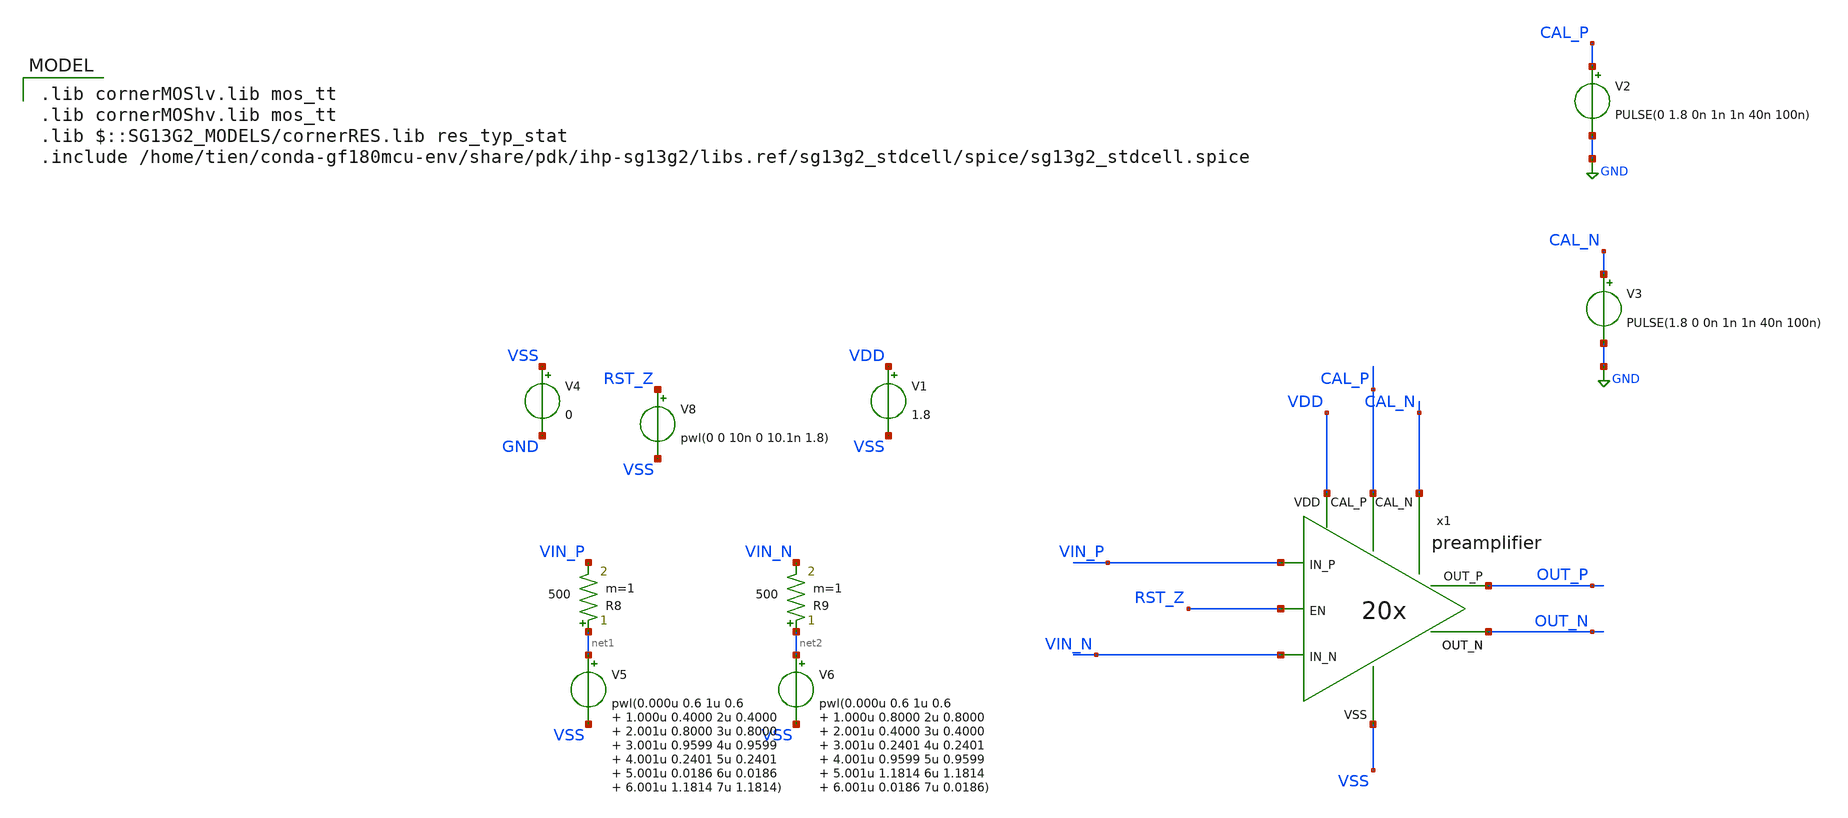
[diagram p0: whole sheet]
** sch_path: schematic/simulations/preamplifier_tb.sch
**.subckt preamplifier_tb
V8 RST_Z VSS pwl(0 0 10n 0 10.1n 1.8)
V1 VDD VSS 1.8
.save i(v1)
V4 VSS GND 0
V5 net1 VSS pwl(0.000u 0.6 1u 0.6 1.000u 0.4000 2u 0.4000 2.001u 0.8000 3u 0.8000 3.001u 0.9599 4u
+ 0.9599 4.001u 0.2401 5u 0.2401 5.001u 0.0186 6u 0.0186 6.001u 1.1814 7u 1.1814)
V6 net2 VSS pwl(0.000u 0.6 1u 0.6 1.000u 0.8000 2u 0.8000 2.001u 0.4000 3u 0.4000 3.001u 0.2401 4u
+ 0.2401 4.001u 0.9599 5u 0.9599 5.001u 1.1814 6u 1.1814 6.001u 0.0186 7u 0.0186)
R8 net1 VIN_P 500 m=1
R9 net2 VIN_N 500 m=1
V2 CAL_P GND PULSE(0 1.8 0n 1n 1n 40n 100n)
V3 CAL_N GND PULSE(1.8 0 0n 1n 1n 40n 100n)
x1 VIN_N VIN_P VDD RST_Z OUT_P OUT_N VSS CAL_P CAL_N preamplifier
**** begin user architecture code
 .lib cornerMOSlv.lib mos_tt
.lib cornerMOShv.lib mos_tt
.lib $::SG13G2_MODELS/cornerRES.lib res_typ_stat
.include /home/tien/conda-gf180mcu-env/share/pdk/ihp-sg13g2/libs.ref/sg13g2_stdcell/spice/sg13g2_stdcell.spice




.option temp = 27
.save all

.option GMIN=1e-12 reltol=1e-6

.tran 10n 10u


**** end user architecture code
**.ends

* expanding   symbol:  preamplifier/preamplifier.sym # of pins=9
** sym_path: schematic/preamplifier/preamplifier.sym
** sch_path: schematic/preamplifier/preamplifier.sch
.subckt preamplifier IN_N IN_P VDD EN OUT_P OUT_N VSS CAL_P CAL_N
*.ipin VDD
*.ipin VSS
*.ipin IN_P
*.ipin IN_N
*.opin OUT_P
*.opin OUT_N
*.ipin EN
*.ipin CAL_P
*.ipin CAL_N
XM3 net1 net2 VDD VDD sg13_lv_pmos w=1.058u l=1u ng=1 m=6 mm_ok=1
XM2 net2 EN VDD VDD sg13_lv_pmos w=0.305u l=0.15u ng=1 m=1 mm_ok=1
XM5 VDD net2 VDD VDD sg13_lv_pmos w=1.058u l=1u ng=1 m=2 mm_ok=1
XM6 net4 net2 VDD VDD sg13_lv_pmos w=1.058u l=1u ng=1 m=1 mm_ok=1
XM1 net2 net2 VDD VDD sg13_lv_pmos w=1.058u l=1u ng=1 m=1 mm_ok=1
XM4 net8 net2 VDD VDD sg13_lv_pmos w=1.058u l=1u ng=1 m=3 mm_ok=1
XM7 net11 IN_P net1 VDD sg13_lv_pmos w=4.8u l=0.2u ng=2 m=4 mm_ok=1
XM8 net6 IN_N net1 VDD sg13_lv_pmos w=4.8u l=0.2u ng=2 m=4 mm_ok=1
XM9 OUT_P VSS net6 VDD sg13_hv_pmos w=14.6u l=0.4u ng=2 m=1 mm_ok=1
XM10 OUT_N VSS net11 VDD sg13_hv_pmos w=14.6u l=0.4u ng=2 m=1 mm_ok=1
XM11 net9 CAL_P net8 VDD sg13_lv_pmos w=1u l=1.77u ng=1 m=1 mm_ok=1
XM12 net10 CAL_N net8 VDD sg13_lv_pmos w=1u l=1.77u ng=1 m=1 mm_ok=1
XM13 net10 net5 VSS VSS sg13_lv_nmos w=1.118u l=0.15u ng=1 m=1 mm_ok=1
XM14 net9 net5 VSS VSS sg13_lv_nmos w=1.118u l=0.15u ng=1 m=1 mm_ok=1
XM15 net9 VSS VSS VSS sg13_lv_nmos w=1.118u l=0.15u ng=1 m=1 mm_ok=1
XM16 net10 VSS VSS VSS sg13_lv_nmos w=1.118u l=0.15u ng=1 m=1 mm_ok=1
XM17 net3 net3 VSS VSS sg13_lv_nmos w=0.9u l=0.15u ng=1 m=1 mm_ok=1
XM18 net5 net3 VSS VSS sg13_lv_nmos w=0.9u l=0.15u ng=1 m=2 mm_ok=1
XM19 VSS net3 VSS VSS sg13_lv_nmos w=0.9u l=0.15u ng=1 m=2 mm_ok=1
x1 EN_Z EN VDD VSS sg13g2_inv_1
XM20 OUT_P net4 net10 VSS sg13_lv_nmos w=0.9u l=0.15u ng=1 m=4 mm_ok=1
XM21 OUT_N net4 net9 VSS sg13_lv_nmos w=0.9u l=0.15u ng=1 m=4 mm_ok=1
XM22 net7 EN VSS VSS sg13_lv_nmos w=3.5u l=0.15u ng=1 m=1 mm_ok=1
XM23 net4 EN_Z VSS VSS sg13_lv_nmos w=0.42u l=0.15u ng=1 m=1 mm_ok=1
XM24 VDD OUT_N net5 VSS sg13_hv_nmos w=0.69u l=0.5u ng=1 m=1 rfmode=1 mm_ok=1
XM25 VDD OUT_P net5 VSS sg13_hv_nmos w=0.69u l=0.5u ng=1 m=1 rfmode=1 mm_ok=1
XR3 OUT_N rn[0] gnd rhigh w=0.5e-6 l=2.75e-6 m=1 b=0 mm_ok=1
XR1 rp[0] OUT_P gnd rhigh w=0.5e-6 l=2.75e-6 m=1 b=0 mm_ok=1
XR2 net14 net7 gnd rhigh w=0.5e-6 l=2.75e-6 m=1 b=0 mm_ok=1
XR4 net13 net14 gnd rhigh w=0.5e-6 l=2.75e-6 m=1 b=0 mm_ok=1
XR5 net12 net13 gnd rhigh w=0.5e-6 l=2.75e-6 m=1 b=0 mm_ok=1
XR6 net2 net12 gnd rhigh w=0.5e-6 l=2.75e-6 m=1 b=0 mm_ok=1
XR7 net15 net3 gnd rhigh w=0.5e-6 l=2.75e-6 m=1 b=0 mm_ok=1
XR8 net4 net15 gnd rhigh w=0.5e-6 l=2.75e-6 m=1 b=0 mm_ok=1
.ends


* expanding   symbol:  sg13g2_stdcells/sg13g2_inv_1.sym # of pins=2
** sym_path: sg13g2_stdcells/sg13g2_inv_1.sym
** sch_path: sg13g2_stdcells/sg13g2_inv_1.sch
.subckt sg13g2_inv_1 Y A VDD VSS
*.opin Y
*.ipin A
*.iopin VDD
*.iopin VSS
XM1 Y A VSS VSS sg13_lv_nmos w=740.00n l=130.00n ng=1 m=1 mm_ok=1
XM2 Y A VDD VDD sg13_lv_pmos w=1.12u l=130.00n ng=1 m=1 mm_ok=1
.ends

.GLOBAL GND
.end
